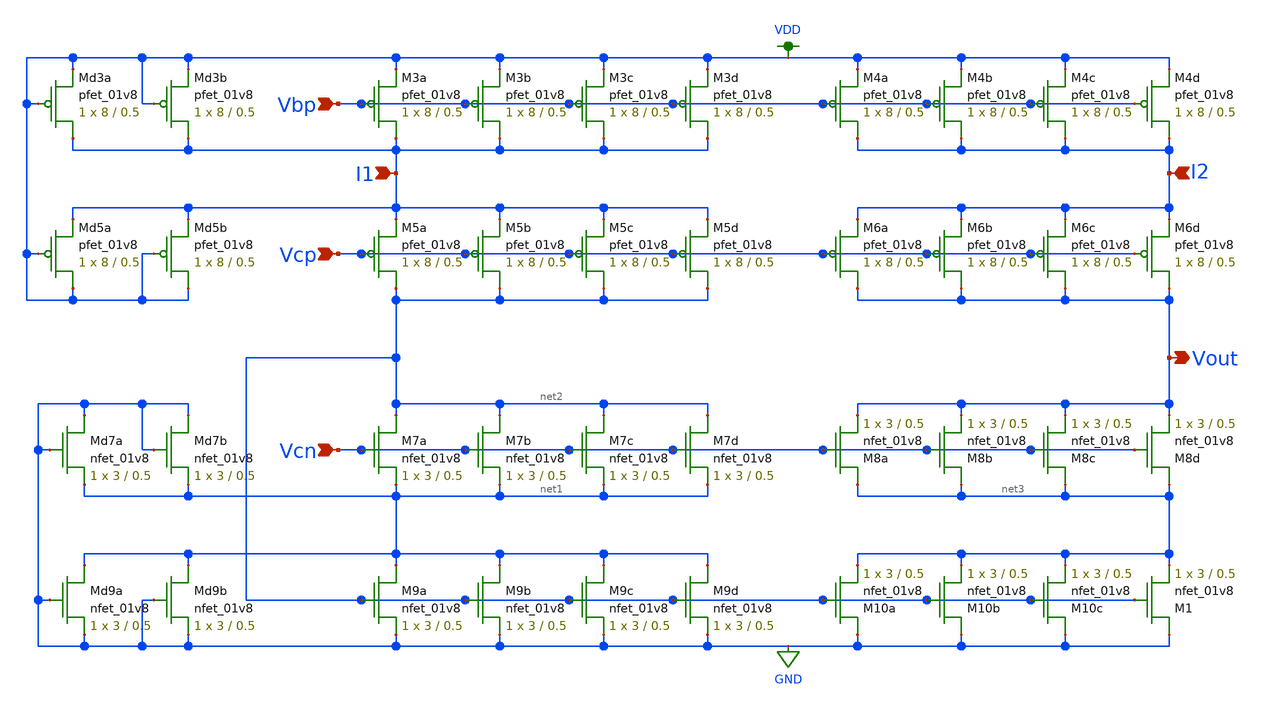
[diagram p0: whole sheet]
** sch_path: xschem/current_difference_balanced.sch
**.subckt current_difference_balanced Vbp Vcp Vcn I2 I1 Vout
*.ipin Vbp
*.ipin Vcp
*.ipin Vcn
*.ipin I2
*.ipin I1
*.opin Vout
XM7a net2 Vcn net1 GND sky130_fd_pr__nfet_01v8 L=0.5 W=3 nf=1 ad='int((nf+1)/2) * W/nf * 0.29' as='int((nf+2)/2) * W/nf * 0.29'
+ pd='2*int((nf+1)/2) * (W/nf + 0.29)' ps='2*int((nf+2)/2) * (W/nf + 0.29)' nrd='0.29 / W' nrs='0.29 / W'
+ sa=0 sb=0 sd=0 mult=1 m=1
XM7b net2 Vcn net1 GND sky130_fd_pr__nfet_01v8 L=0.5 W=3 nf=1 ad='int((nf+1)/2) * W/nf * 0.29' as='int((nf+2)/2) * W/nf * 0.29'
+ pd='2*int((nf+1)/2) * (W/nf + 0.29)' ps='2*int((nf+2)/2) * (W/nf + 0.29)' nrd='0.29 / W' nrs='0.29 / W'
+ sa=0 sb=0 sd=0 mult=1 m=1
XM7c net2 Vcn net1 GND sky130_fd_pr__nfet_01v8 L=0.5 W=3 nf=1 ad='int((nf+1)/2) * W/nf * 0.29' as='int((nf+2)/2) * W/nf * 0.29'
+ pd='2*int((nf+1)/2) * (W/nf + 0.29)' ps='2*int((nf+2)/2) * (W/nf + 0.29)' nrd='0.29 / W' nrs='0.29 / W'
+ sa=0 sb=0 sd=0 mult=1 m=1
XM7d net2 Vcn net1 GND sky130_fd_pr__nfet_01v8 L=0.5 W=3 nf=1 ad='int((nf+1)/2) * W/nf * 0.29' as='int((nf+2)/2) * W/nf * 0.29'
+ pd='2*int((nf+1)/2) * (W/nf + 0.29)' ps='2*int((nf+2)/2) * (W/nf + 0.29)' nrd='0.29 / W' nrs='0.29 / W'
+ sa=0 sb=0 sd=0 mult=1 m=1
XM8a net3 Vcn Vout GND sky130_fd_pr__nfet_01v8 L=0.5 W=3 nf=1 ad='int((nf+1)/2) * W/nf * 0.29' as='int((nf+2)/2) * W/nf * 0.29'
+ pd='2*int((nf+1)/2) * (W/nf + 0.29)' ps='2*int((nf+2)/2) * (W/nf + 0.29)' nrd='0.29 / W' nrs='0.29 / W'
+ sa=0 sb=0 sd=0 mult=1 m=1
XM8b net3 Vcn Vout GND sky130_fd_pr__nfet_01v8 L=0.5 W=3 nf=1 ad='int((nf+1)/2) * W/nf * 0.29' as='int((nf+2)/2) * W/nf * 0.29'
+ pd='2*int((nf+1)/2) * (W/nf + 0.29)' ps='2*int((nf+2)/2) * (W/nf + 0.29)' nrd='0.29 / W' nrs='0.29 / W'
+ sa=0 sb=0 sd=0 mult=1 m=1
XM8c net3 Vcn Vout GND sky130_fd_pr__nfet_01v8 L=0.5 W=3 nf=1 ad='int((nf+1)/2) * W/nf * 0.29' as='int((nf+2)/2) * W/nf * 0.29'
+ pd='2*int((nf+1)/2) * (W/nf + 0.29)' ps='2*int((nf+2)/2) * (W/nf + 0.29)' nrd='0.29 / W' nrs='0.29 / W'
+ sa=0 sb=0 sd=0 mult=1 m=1
XM8d net3 Vcn Vout GND sky130_fd_pr__nfet_01v8 L=0.5 W=3 nf=1 ad='int((nf+1)/2) * W/nf * 0.29' as='int((nf+2)/2) * W/nf * 0.29'
+ pd='2*int((nf+1)/2) * (W/nf + 0.29)' ps='2*int((nf+2)/2) * (W/nf + 0.29)' nrd='0.29 / W' nrs='0.29 / W'
+ sa=0 sb=0 sd=0 mult=1 m=1
XM9a net1 net2 GND GND sky130_fd_pr__nfet_01v8 L=0.5 W=3 nf=1 ad='int((nf+1)/2) * W/nf * 0.29' as='int((nf+2)/2) * W/nf * 0.29'
+ pd='2*int((nf+1)/2) * (W/nf + 0.29)' ps='2*int((nf+2)/2) * (W/nf + 0.29)' nrd='0.29 / W' nrs='0.29 / W'
+ sa=0 sb=0 sd=0 mult=1 m=1
XM9b net1 net2 GND GND sky130_fd_pr__nfet_01v8 L=0.5 W=3 nf=1 ad='int((nf+1)/2) * W/nf * 0.29' as='int((nf+2)/2) * W/nf * 0.29'
+ pd='2*int((nf+1)/2) * (W/nf + 0.29)' ps='2*int((nf+2)/2) * (W/nf + 0.29)' nrd='0.29 / W' nrs='0.29 / W'
+ sa=0 sb=0 sd=0 mult=1 m=1
XM9c net1 net2 GND GND sky130_fd_pr__nfet_01v8 L=0.5 W=3 nf=1 ad='int((nf+1)/2) * W/nf * 0.29' as='int((nf+2)/2) * W/nf * 0.29'
+ pd='2*int((nf+1)/2) * (W/nf + 0.29)' ps='2*int((nf+2)/2) * (W/nf + 0.29)' nrd='0.29 / W' nrs='0.29 / W'
+ sa=0 sb=0 sd=0 mult=1 m=1
XM9d net1 net2 GND GND sky130_fd_pr__nfet_01v8 L=0.5 W=3 nf=1 ad='int((nf+1)/2) * W/nf * 0.29' as='int((nf+2)/2) * W/nf * 0.29'
+ pd='2*int((nf+1)/2) * (W/nf + 0.29)' ps='2*int((nf+2)/2) * (W/nf + 0.29)' nrd='0.29 / W' nrs='0.29 / W'
+ sa=0 sb=0 sd=0 mult=1 m=1
XM10a GND net2 net3 GND sky130_fd_pr__nfet_01v8 L=0.5 W=3 nf=1 ad='int((nf+1)/2) * W/nf * 0.29' as='int((nf+2)/2) * W/nf * 0.29'
+ pd='2*int((nf+1)/2) * (W/nf + 0.29)' ps='2*int((nf+2)/2) * (W/nf + 0.29)' nrd='0.29 / W' nrs='0.29 / W'
+ sa=0 sb=0 sd=0 mult=1 m=1
XM10b GND net2 net3 GND sky130_fd_pr__nfet_01v8 L=0.5 W=3 nf=1 ad='int((nf+1)/2) * W/nf * 0.29' as='int((nf+2)/2) * W/nf * 0.29'
+ pd='2*int((nf+1)/2) * (W/nf + 0.29)' ps='2*int((nf+2)/2) * (W/nf + 0.29)' nrd='0.29 / W' nrs='0.29 / W'
+ sa=0 sb=0 sd=0 mult=1 m=1
XM10c GND net2 net3 GND sky130_fd_pr__nfet_01v8 L=0.5 W=3 nf=1 ad='int((nf+1)/2) * W/nf * 0.29' as='int((nf+2)/2) * W/nf * 0.29'
+ pd='2*int((nf+1)/2) * (W/nf + 0.29)' ps='2*int((nf+2)/2) * (W/nf + 0.29)' nrd='0.29 / W' nrs='0.29 / W'
+ sa=0 sb=0 sd=0 mult=1 m=1
XM1 GND net2 net3 GND sky130_fd_pr__nfet_01v8 L=0.5 W=3 nf=1 ad='int((nf+1)/2) * W/nf * 0.29' as='int((nf+2)/2) * W/nf * 0.29'
+ pd='2*int((nf+1)/2) * (W/nf + 0.29)' ps='2*int((nf+2)/2) * (W/nf + 0.29)' nrd='0.29 / W' nrs='0.29 / W'
+ sa=0 sb=0 sd=0 mult=1 m=1
XM5a net2 Vcp I1 VDD sky130_fd_pr__pfet_01v8 L=0.5 W=8 nf=1 ad='int((nf+1)/2) * W/nf * 0.29' as='int((nf+2)/2) * W/nf * 0.29'
+ pd='2*int((nf+1)/2) * (W/nf + 0.29)' ps='2*int((nf+2)/2) * (W/nf + 0.29)' nrd='0.29 / W' nrs='0.29 / W'
+ sa=0 sb=0 sd=0 mult=1 m=1
XM5b net2 Vcp I1 VDD sky130_fd_pr__pfet_01v8 L=0.5 W=8 nf=1 ad='int((nf+1)/2) * W/nf * 0.29' as='int((nf+2)/2) * W/nf * 0.29'
+ pd='2*int((nf+1)/2) * (W/nf + 0.29)' ps='2*int((nf+2)/2) * (W/nf + 0.29)' nrd='0.29 / W' nrs='0.29 / W'
+ sa=0 sb=0 sd=0 mult=1 m=1
XM5c net2 Vcp I1 VDD sky130_fd_pr__pfet_01v8 L=0.5 W=8 nf=1 ad='int((nf+1)/2) * W/nf * 0.29' as='int((nf+2)/2) * W/nf * 0.29'
+ pd='2*int((nf+1)/2) * (W/nf + 0.29)' ps='2*int((nf+2)/2) * (W/nf + 0.29)' nrd='0.29 / W' nrs='0.29 / W'
+ sa=0 sb=0 sd=0 mult=1 m=1
XM5d net2 Vcp I1 VDD sky130_fd_pr__pfet_01v8 L=0.5 W=8 nf=1 ad='int((nf+1)/2) * W/nf * 0.29' as='int((nf+2)/2) * W/nf * 0.29'
+ pd='2*int((nf+1)/2) * (W/nf + 0.29)' ps='2*int((nf+2)/2) * (W/nf + 0.29)' nrd='0.29 / W' nrs='0.29 / W'
+ sa=0 sb=0 sd=0 mult=1 m=1
XM6a Vout Vcp I2 VDD sky130_fd_pr__pfet_01v8 L=0.5 W=8 nf=1 ad='int((nf+1)/2) * W/nf * 0.29' as='int((nf+2)/2) * W/nf * 0.29'
+ pd='2*int((nf+1)/2) * (W/nf + 0.29)' ps='2*int((nf+2)/2) * (W/nf + 0.29)' nrd='0.29 / W' nrs='0.29 / W'
+ sa=0 sb=0 sd=0 mult=1 m=1
XM6b Vout Vcp I2 VDD sky130_fd_pr__pfet_01v8 L=0.5 W=8 nf=1 ad='int((nf+1)/2) * W/nf * 0.29' as='int((nf+2)/2) * W/nf * 0.29'
+ pd='2*int((nf+1)/2) * (W/nf + 0.29)' ps='2*int((nf+2)/2) * (W/nf + 0.29)' nrd='0.29 / W' nrs='0.29 / W'
+ sa=0 sb=0 sd=0 mult=1 m=1
XM6c Vout Vcp I2 VDD sky130_fd_pr__pfet_01v8 L=0.5 W=8 nf=1 ad='int((nf+1)/2) * W/nf * 0.29' as='int((nf+2)/2) * W/nf * 0.29'
+ pd='2*int((nf+1)/2) * (W/nf + 0.29)' ps='2*int((nf+2)/2) * (W/nf + 0.29)' nrd='0.29 / W' nrs='0.29 / W'
+ sa=0 sb=0 sd=0 mult=1 m=1
XM6d Vout Vcp I2 VDD sky130_fd_pr__pfet_01v8 L=0.5 W=8 nf=1 ad='int((nf+1)/2) * W/nf * 0.29' as='int((nf+2)/2) * W/nf * 0.29'
+ pd='2*int((nf+1)/2) * (W/nf + 0.29)' ps='2*int((nf+2)/2) * (W/nf + 0.29)' nrd='0.29 / W' nrs='0.29 / W'
+ sa=0 sb=0 sd=0 mult=1 m=1
XM3a I1 Vbp VDD VDD sky130_fd_pr__pfet_01v8 L=0.5 W=8 nf=1 ad='int((nf+1)/2) * W/nf * 0.29' as='int((nf+2)/2) * W/nf * 0.29'
+ pd='2*int((nf+1)/2) * (W/nf + 0.29)' ps='2*int((nf+2)/2) * (W/nf + 0.29)' nrd='0.29 / W' nrs='0.29 / W'
+ sa=0 sb=0 sd=0 mult=1 m=1
XM3b I1 Vbp VDD VDD sky130_fd_pr__pfet_01v8 L=0.5 W=8 nf=1 ad='int((nf+1)/2) * W/nf * 0.29' as='int((nf+2)/2) * W/nf * 0.29'
+ pd='2*int((nf+1)/2) * (W/nf + 0.29)' ps='2*int((nf+2)/2) * (W/nf + 0.29)' nrd='0.29 / W' nrs='0.29 / W'
+ sa=0 sb=0 sd=0 mult=1 m=1
XM3c I1 Vbp VDD VDD sky130_fd_pr__pfet_01v8 L=0.5 W=8 nf=1 ad='int((nf+1)/2) * W/nf * 0.29' as='int((nf+2)/2) * W/nf * 0.29'
+ pd='2*int((nf+1)/2) * (W/nf + 0.29)' ps='2*int((nf+2)/2) * (W/nf + 0.29)' nrd='0.29 / W' nrs='0.29 / W'
+ sa=0 sb=0 sd=0 mult=1 m=1
XM3d I1 Vbp VDD VDD sky130_fd_pr__pfet_01v8 L=0.5 W=8 nf=1 ad='int((nf+1)/2) * W/nf * 0.29' as='int((nf+2)/2) * W/nf * 0.29'
+ pd='2*int((nf+1)/2) * (W/nf + 0.29)' ps='2*int((nf+2)/2) * (W/nf + 0.29)' nrd='0.29 / W' nrs='0.29 / W'
+ sa=0 sb=0 sd=0 mult=1 m=1
XM4a I2 Vbp VDD VDD sky130_fd_pr__pfet_01v8 L=0.5 W=8 nf=1 ad='int((nf+1)/2) * W/nf * 0.29' as='int((nf+2)/2) * W/nf * 0.29'
+ pd='2*int((nf+1)/2) * (W/nf + 0.29)' ps='2*int((nf+2)/2) * (W/nf + 0.29)' nrd='0.29 / W' nrs='0.29 / W'
+ sa=0 sb=0 sd=0 mult=1 m=1
XM4b I2 Vbp VDD VDD sky130_fd_pr__pfet_01v8 L=0.5 W=8 nf=1 ad='int((nf+1)/2) * W/nf * 0.29' as='int((nf+2)/2) * W/nf * 0.29'
+ pd='2*int((nf+1)/2) * (W/nf + 0.29)' ps='2*int((nf+2)/2) * (W/nf + 0.29)' nrd='0.29 / W' nrs='0.29 / W'
+ sa=0 sb=0 sd=0 mult=1 m=1
XM4c I2 Vbp VDD VDD sky130_fd_pr__pfet_01v8 L=0.5 W=8 nf=1 ad='int((nf+1)/2) * W/nf * 0.29' as='int((nf+2)/2) * W/nf * 0.29'
+ pd='2*int((nf+1)/2) * (W/nf + 0.29)' ps='2*int((nf+2)/2) * (W/nf + 0.29)' nrd='0.29 / W' nrs='0.29 / W'
+ sa=0 sb=0 sd=0 mult=1 m=1
XM4d I2 Vbp VDD VDD sky130_fd_pr__pfet_01v8 L=0.5 W=8 nf=1 ad='int((nf+1)/2) * W/nf * 0.29' as='int((nf+2)/2) * W/nf * 0.29'
+ pd='2*int((nf+1)/2) * (W/nf + 0.29)' ps='2*int((nf+2)/2) * (W/nf + 0.29)' nrd='0.29 / W' nrs='0.29 / W'
+ sa=0 sb=0 sd=0 mult=1 m=1
XMd3b I1 VDD VDD VDD sky130_fd_pr__pfet_01v8 L=0.5 W=8 nf=1 ad='int((nf+1)/2) * W/nf * 0.29' as='int((nf+2)/2) * W/nf * 0.29'
+ pd='2*int((nf+1)/2) * (W/nf + 0.29)' ps='2*int((nf+2)/2) * (W/nf + 0.29)' nrd='0.29 / W' nrs='0.29 / W'
+ sa=0 sb=0 sd=0 mult=1 m=1
XMd3a I1 VDD VDD VDD sky130_fd_pr__pfet_01v8 L=0.5 W=8 nf=1 ad='int((nf+1)/2) * W/nf * 0.29' as='int((nf+2)/2) * W/nf * 0.29'
+ pd='2*int((nf+1)/2) * (W/nf + 0.29)' ps='2*int((nf+2)/2) * (W/nf + 0.29)' nrd='0.29 / W' nrs='0.29 / W'
+ sa=0 sb=0 sd=0 mult=1 m=1
XMd5b VDD VDD I1 VDD sky130_fd_pr__pfet_01v8 L=0.5 W=8 nf=1 ad='int((nf+1)/2) * W/nf * 0.29' as='int((nf+2)/2) * W/nf * 0.29'
+ pd='2*int((nf+1)/2) * (W/nf + 0.29)' ps='2*int((nf+2)/2) * (W/nf + 0.29)' nrd='0.29 / W' nrs='0.29 / W'
+ sa=0 sb=0 sd=0 mult=1 m=1
XMd5a VDD VDD I1 VDD sky130_fd_pr__pfet_01v8 L=0.5 W=8 nf=1 ad='int((nf+1)/2) * W/nf * 0.29' as='int((nf+2)/2) * W/nf * 0.29'
+ pd='2*int((nf+1)/2) * (W/nf + 0.29)' ps='2*int((nf+2)/2) * (W/nf + 0.29)' nrd='0.29 / W' nrs='0.29 / W'
+ sa=0 sb=0 sd=0 mult=1 m=1
XMd7a GND GND net1 GND sky130_fd_pr__nfet_01v8 L=0.5 W=3 nf=1 ad='int((nf+1)/2) * W/nf * 0.29' as='int((nf+2)/2) * W/nf * 0.29'
+ pd='2*int((nf+1)/2) * (W/nf + 0.29)' ps='2*int((nf+2)/2) * (W/nf + 0.29)' nrd='0.29 / W' nrs='0.29 / W'
+ sa=0 sb=0 sd=0 mult=1 m=1
XMd7b GND GND net1 GND sky130_fd_pr__nfet_01v8 L=0.5 W=3 nf=1 ad='int((nf+1)/2) * W/nf * 0.29' as='int((nf+2)/2) * W/nf * 0.29'
+ pd='2*int((nf+1)/2) * (W/nf + 0.29)' ps='2*int((nf+2)/2) * (W/nf + 0.29)' nrd='0.29 / W' nrs='0.29 / W'
+ sa=0 sb=0 sd=0 mult=1 m=1
XMd9a net1 GND GND GND sky130_fd_pr__nfet_01v8 L=0.5 W=3 nf=1 ad='int((nf+1)/2) * W/nf * 0.29' as='int((nf+2)/2) * W/nf * 0.29'
+ pd='2*int((nf+1)/2) * (W/nf + 0.29)' ps='2*int((nf+2)/2) * (W/nf + 0.29)' nrd='0.29 / W' nrs='0.29 / W'
+ sa=0 sb=0 sd=0 mult=1 m=1
XMd9b net1 GND GND GND sky130_fd_pr__nfet_01v8 L=0.5 W=3 nf=1 ad='int((nf+1)/2) * W/nf * 0.29' as='int((nf+2)/2) * W/nf * 0.29'
+ pd='2*int((nf+1)/2) * (W/nf + 0.29)' ps='2*int((nf+2)/2) * (W/nf + 0.29)' nrd='0.29 / W' nrs='0.29 / W'
+ sa=0 sb=0 sd=0 mult=1 m=1
**.ends
.GLOBAL VDD
.GLOBAL GND
.end
